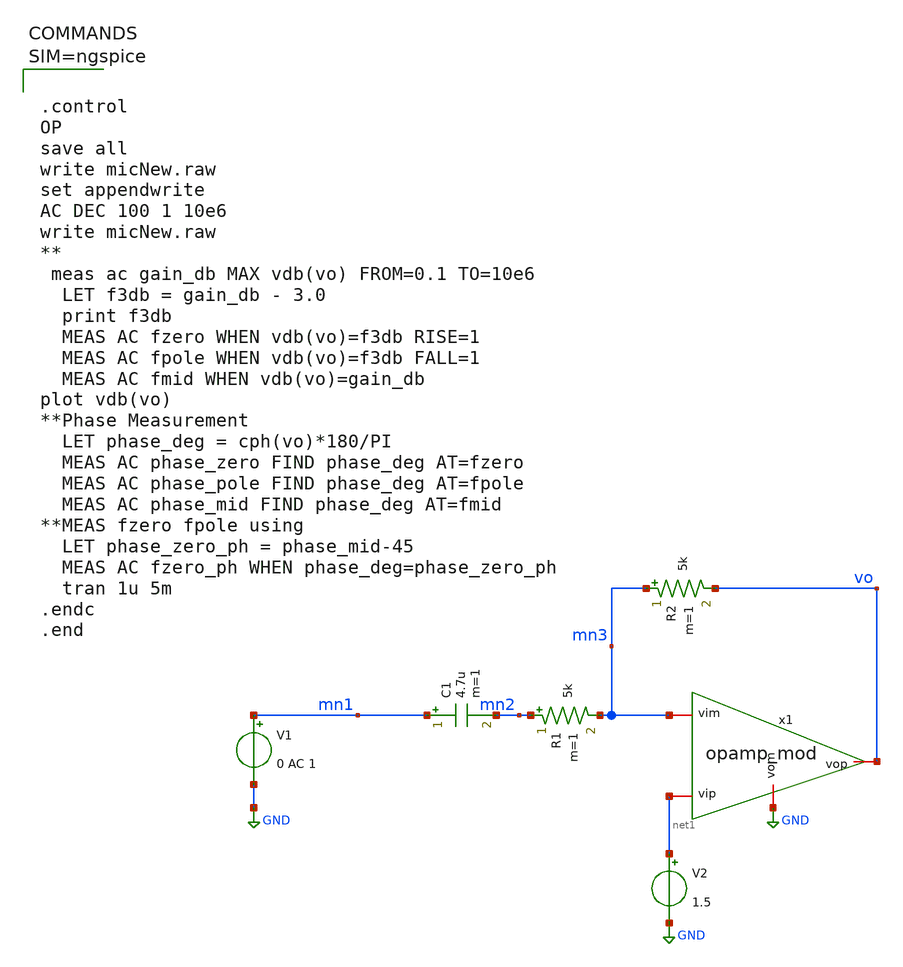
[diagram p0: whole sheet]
** sch_path: xschem/micNewOpa_mod1.sch
**.subckt micNewOpa_mod1
V1 mn1 GND 0 AC 1
C1 mn1 mn2 4.7u m=1
R1 mn2 mn3 5k m=1
R2 mn3 vo 5k m=1
V2 net1 GND 1.5
x1 vo net1 mn3 GND opamp_mod
**** begin user architecture code



.control
OP
save all
write micNew.raw
set appendwrite
AC DEC 100 1 10e6
write micNew.raw
**
 meas ac gain_db MAX vdb(vo) FROM=0.1 TO=10e6
  LET f3db = gain_db - 3.0
  print f3db
  MEAS AC fzero WHEN vdb(vo)=f3db RISE=1
  MEAS AC fpole WHEN vdb(vo)=f3db FALL=1
  MEAS AC fmid WHEN vdb(vo)=gain_db
plot vdb(vo)
**Phase Measurement
  LET phase_deg = cph(vo)*180/PI
  MEAS AC phase_zero FIND phase_deg AT=fzero
  MEAS AC phase_pole FIND phase_deg AT=fpole
  MEAS AC phase_mid FIND phase_deg AT=fmid
**MEAS fzero fpole using
  LET phase_zero_ph = phase_mid-45
  MEAS AC fzero_ph WHEN phase_deg=phase_zero_ph
  tran 1u 5m
.endc
.end



**** end user architecture code
**.ends

* expanding   symbol:  opamp_mod.sym # of pins=4
** sym_path: xschem/opamp_mod.sym
** sch_path: xschem/opamp_mod.sch
.subckt opamp_mod vop vip vim vom
*.iopin vop
*.iopin vom
*.iopin vip
*.iopin vim
E1 vop vom vip vim 1000
.ends

.GLOBAL GND
.end
